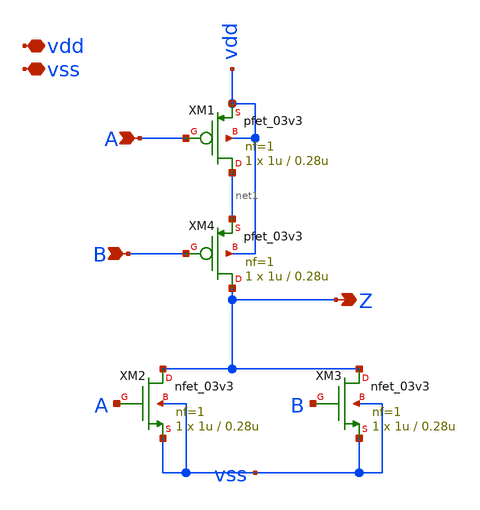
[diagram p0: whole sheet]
** sch_path: designs/libs/core_LIF_comp/core_nor/nor.sch
**.subckt nor vdd vss A Z B
*.iopin vdd
*.iopin vss
*.ipin A
*.opin Z
*.ipin B
XM1 net1 A vdd vdd pfet_03v3 L=0.28u W=1u nf=1 ad='int((nf+1)/2) * W/nf * 0.18u' as='int((nf+2)/2) * W/nf * 0.18u'
+ pd='2*int((nf+1)/2) * (W/nf + 0.18u)' ps='2*int((nf+2)/2) * (W/nf + 0.18u)' nrd='0.18u / W' nrs='0.18u / W'
+ sa=0 sb=0 sd=0 m=1
XM3 Z B vss vss nfet_03v3 L=0.28u W=1u nf=1 ad='int((nf+1)/2) * W/nf * 0.18u' as='int((nf+2)/2) * W/nf * 0.18u'
+ pd='2*int((nf+1)/2) * (W/nf + 0.18u)' ps='2*int((nf+2)/2) * (W/nf + 0.18u)' nrd='0.18u / W' nrs='0.18u / W'
+ sa=0 sb=0 sd=0 m=1
XM2 Z A vss vss nfet_03v3 L=0.28u W=1u nf=1 ad='int((nf+1)/2) * W/nf * 0.18u' as='int((nf+2)/2) * W/nf * 0.18u'
+ pd='2*int((nf+1)/2) * (W/nf + 0.18u)' ps='2*int((nf+2)/2) * (W/nf + 0.18u)' nrd='0.18u / W' nrs='0.18u / W'
+ sa=0 sb=0 sd=0 m=1
XM4 Z B net1 vdd pfet_03v3 L=0.28u W=1u nf=1 ad='int((nf+1)/2) * W/nf * 0.18u' as='int((nf+2)/2) * W/nf * 0.18u'
+ pd='2*int((nf+1)/2) * (W/nf + 0.18u)' ps='2*int((nf+2)/2) * (W/nf + 0.18u)' nrd='0.18u / W' nrs='0.18u / W'
+ sa=0 sb=0 sd=0 m=1
**.ends
.end
